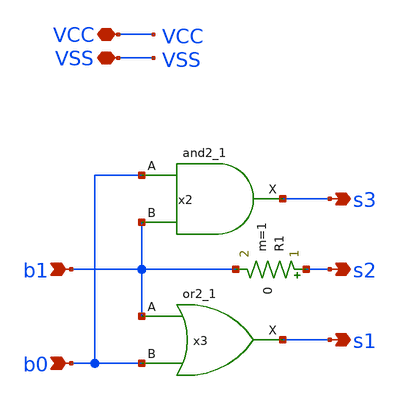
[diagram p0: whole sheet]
** sch_path: xschem/thermo2bit.sch
**.subckt thermo2bit b1 s2 b0 s1 s3 VCC VSS
*.ipin b1
*.opin s2
*.ipin b0
*.opin s1
*.opin s3
*.iopin VCC
*.iopin VSS
x2 b0 b1 VSS VSS VCC VCC s3 sky130_fd_sc_hd__and2_1
x3 b1 b0 VSS VSS VCC VCC s1 sky130_fd_sc_hd__or2_1
R1 s2 b1 0 m=1
**.ends
.end
